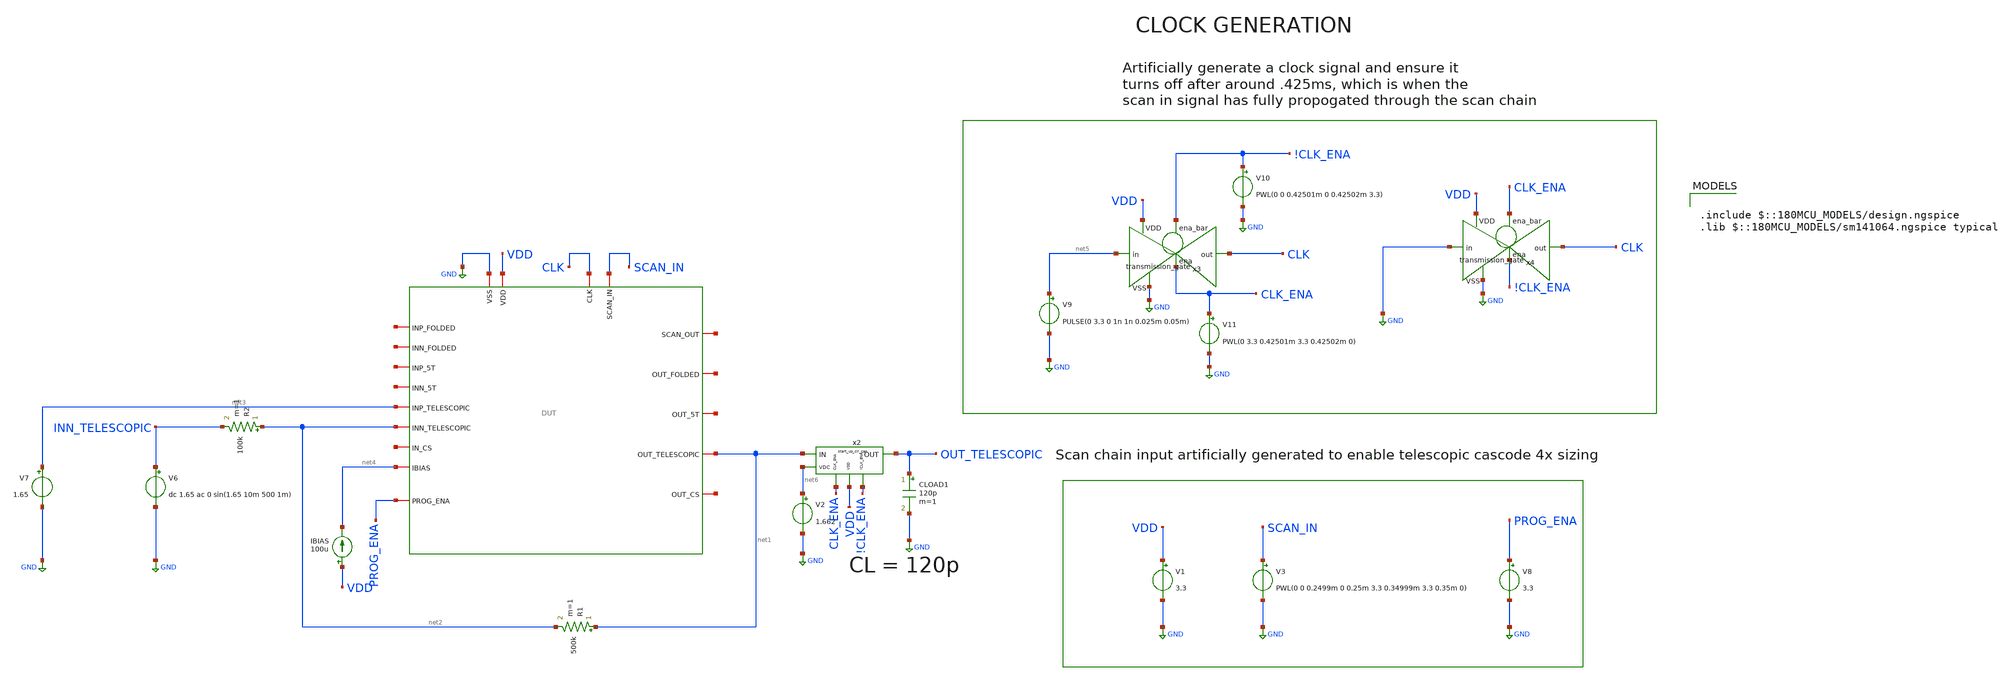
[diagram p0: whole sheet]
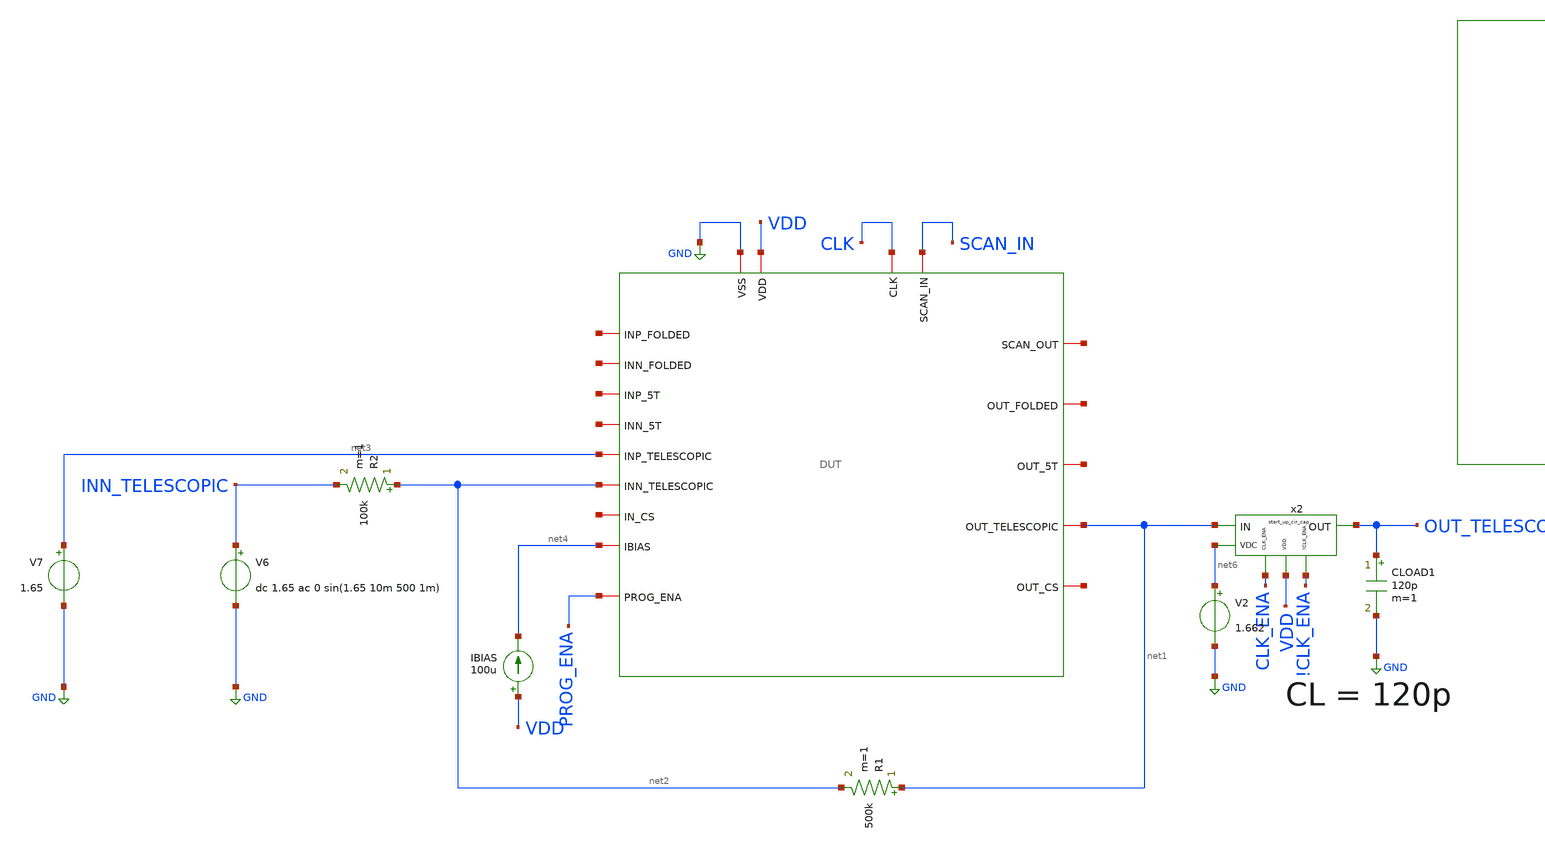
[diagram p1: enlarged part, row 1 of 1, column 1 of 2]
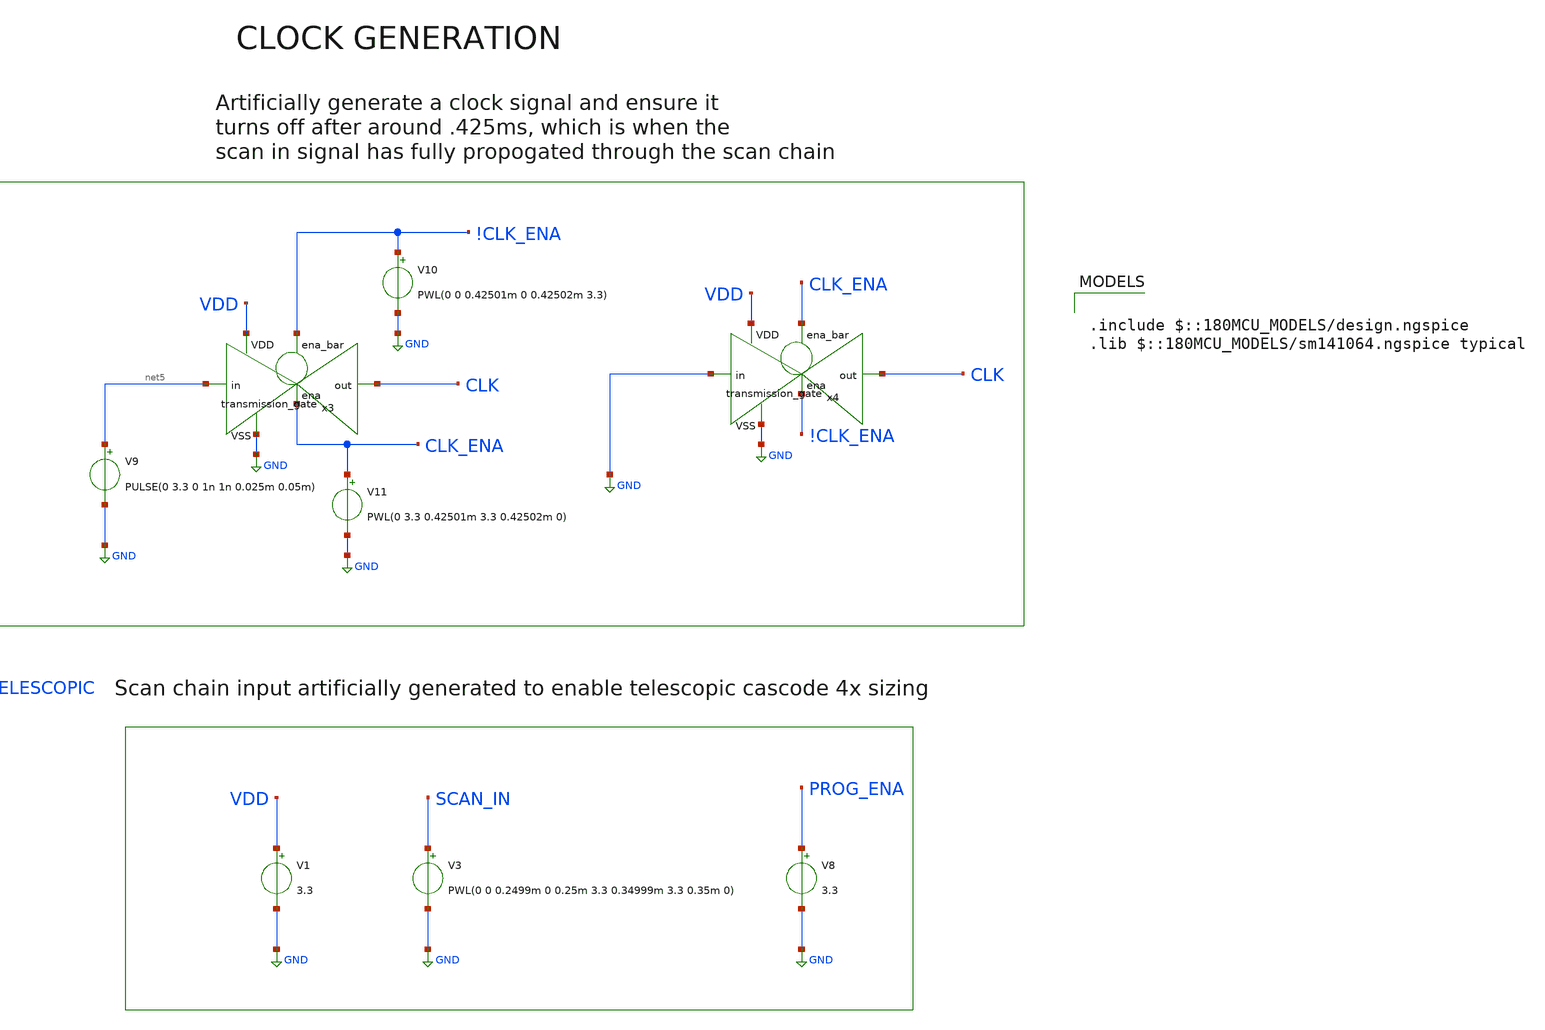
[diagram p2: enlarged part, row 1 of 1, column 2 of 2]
** sch_path: designs/libs/pex/start_up_cir/tele/4x.sch
**.subckt 4x
R1 net1 net2 500k m=1
R2 net2 INN_TELESCOPIC 100k m=1
V6 INN_TELESCOPIC GND dc 1.65 ac 0 sin(1.65 10m 500 1m)
V7 net3 GND 1.65
IBIAS VDD net4 100u
V3 SCAN_IN GND PWL(0 0 0.2499m 0 0.25m 3.3 0.34999m 3.3 0.35m 0)
V1 VDD GND 3.3
V8 PROG_ENA GND 3.3
V9 net5 GND PULSE(0 3.3 0 1n 1n 0.025m 0.05m)
x3 !CLK_ENA VDD CLK net5 GND CLK_ENA transmission_gate
V10 !CLK_ENA GND PWL(0 0 0.42501m 0 0.42502m 3.3)
V11 CLK_ENA GND PWL(0 3.3 0.42501m 3.3 0.42502m 0)
x4 CLK_ENA VDD CLK GND GND !CLK_ENA transmission_gate
x1 CLK net7 SCAN_IN GND VDD net8 net9 net10 net4 net11 net12 net13 net3 net1 net14 net15 net2
+ PROG_ENA DUT
CLOAD1 OUT_TELESCOPIC GND 120p m=1
V2 net6 GND 1.662
x2 CLK_ENA VDD !CLK_ENA net1 OUT_TELESCOPIC net6 start_up_cir_cap
**** begin user architecture code

.include $::180MCU_MODELS/design.ngspice
.lib $::180MCU_MODELS/sm141064.ngspice typical



.include /foss/designs/libs/pex/DUT.spice
.control
tran 1u 5m

plot v(out_telescopic) v(inn_telescopic)
wrdata /foss/designs/libs/pex/start_up_cir/tele/4x.csv v(out_telescopic) v(inn_telescopic)

meas tran vout_pp pp v(out_telescopic) from=2m to=5m
meas tran vin_pp pp v(inn_telescopic) from=2m to=5m
let gain = vout_pp / vin_pp
print gain

meas tran vout_dc avg v(out_telescopic) from=2m to=5m
meas tran vin_dc avg v(inn_telescopic) from=2m to=5m
let dc_offset = vout_dc - vin_dc
let input_offset = dc_offset / 6
print vout_dc vin_dc dc_offset input_offset

let ideal_gain = 5
let gain_error_pct = (ideal_gain - gain) / ideal_gain * 100
print gain_error_pct

meas tran idd avg i(v1) from=2m to=5m
let power = abs(idd) * 3.3
print idd power
.endc


**** end user architecture code
**.ends

* expanding   symbol:  libs/core_digital/schem/transmission_gate.sym # of pins=6
** sym_path: designs/libs/core_digital/schem/transmission_gate.sym
** sch_path: designs/libs/core_digital/schem/transmission_gate.sch
.subckt transmission_gate ena_bar VDD out in VSS ena
*.ipin in
*.ipin ena_bar
*.ipin ena
*.ipin VSS
*.ipin VDD
*.opin out
XM1 in ena_bar out VDD pfet_03v3 L=0.28u W=0.22u nf=1 ad='int((nf+1)/2) * W/nf * 0.18u' as='int((nf+2)/2) * W/nf * 0.18u'
+ pd='2*int((nf+1)/2) * (W/nf + 0.18u)' ps='2*int((nf+2)/2) * (W/nf + 0.18u)' nrd='0.18u / W' nrs='0.18u / W'
+ sa=0 sb=0 sd=0 m=1
XM2 in ena out VSS nfet_03v3 L=0.28u W=0.22u nf=1 ad='int((nf+1)/2) * W/nf * 0.18u' as='int((nf+2)/2) * W/nf * 0.18u'
+ pd='2*int((nf+1)/2) * (W/nf + 0.18u)' ps='2*int((nf+2)/2) * (W/nf + 0.18u)' nrd='0.18u / W' nrs='0.18u / W'
+ sa=0 sb=0 sd=0 m=1
.ends


* expanding   symbol:  libs/core_amps/start_up_cir/start_up_cir_cap.sym # of pins=6
** sym_path: designs/libs/core_amps/start_up_cir/start_up_cir_cap.sym
** sch_path: designs/libs/core_amps/start_up_cir/start_up_cir_cap.sch
.subckt start_up_cir_cap CLK_ENA VDD !CLK_ENA IN OUT VDC
*.ipin IN
*.opin OUT
*.ipin VDC
*.ipin VDD
*.ipin CLK_ENA
*.ipin !CLK_ENA
x2 !CLK_ENA VDD OUT VDC GND CLK_ENA transmission_gate
x5 CLK_ENA VDD OUT IN GND !CLK_ENA transmission_gate
C OUT GND 1n m=1
.ends

.GLOBAL GND
.end
